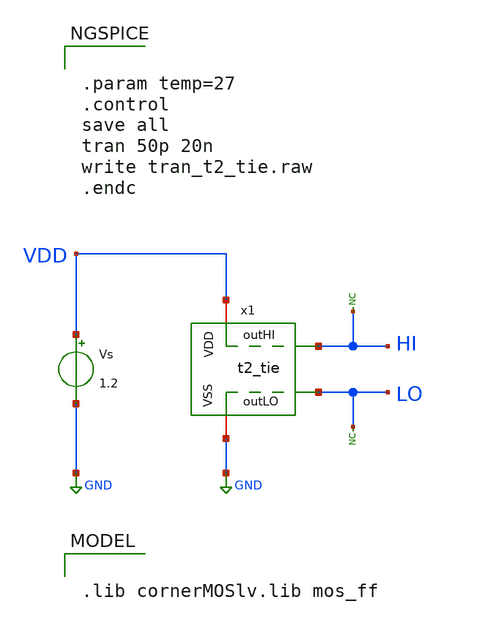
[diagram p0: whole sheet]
** sch_path: Team Designs/Team 2 Design/design_data/xschem/t2_tie_tb.sch
**.subckt t2_tie_tb
Vs VDD GND 1.2
* noconn HI
x1 VDD GND HI LO t2_tie
* noconn LO
**** begin user architecture code


.param temp=27
.control
save all
tran 50p 20n
write tran_t2_tie.raw
.endc



.lib cornerMOSlv.lib mos_ff

**** end user architecture code
**.ends

* expanding   symbol:  t2_tie.sym # of pins=4
** sym_path: Team 2 Design/design_data/xschem/t2_tie.sym
** sch_path: Team 2 Design/design_data/xschem/t2_tie.sch
.subckt t2_tie VDD VSS outHI outLO
*.iopin VSS
*.opin outLO
*.iopin VDD
*.opin outHI
XM1 outHI net1 VDD VDD sg13_lv_pmos w=0.3u l=0.13u ng=1 m=1 mm_ok=1
XM2 net1 net1 VSS VSS sg13_lv_nmos w=0.15u l=0.13u ng=1 m=1 mm_ok=1
XM3 net2 net2 VDD VDD sg13_lv_pmos w=0.3u l=0.13u ng=1 m=1 mm_ok=1
XM4 outLO net2 VSS VSS sg13_lv_nmos w=0.15u l=0.13u ng=1 m=1 mm_ok=1
.ends

.GLOBAL GND
.end
